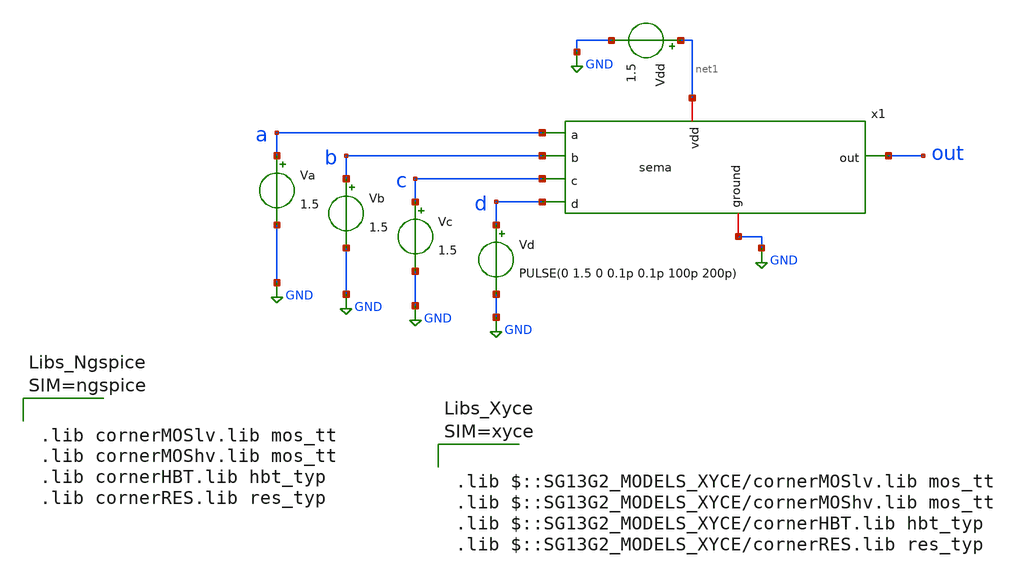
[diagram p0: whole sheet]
** sch_path: projekat/slucaj_3/tb_tran.sch
**.subckt tb_tran
Va a GND 1.5
Vb b GND 1.5
Vc c GND 1.5
Vd d GND PULSE(0 1.5 0 0.1p 0.1p 100p 200p)
Vdd net1 GND 1.5
x1 net1 out d a c b GND sema
**** begin user architecture code



.lib cornerMOSlv.lib mos_tt
.lib cornerMOShv.lib mos_tt
.lib cornerHBT.lib hbt_typ
.lib cornerRES.lib res_typ









.tran 0.1p 500p

.control
  save all
  run

  meas tran tr_out TRIG v(out) VAL=0.15 RISE=2 TARG v(out) VAL=1.35 RISE=2
  meas tran tf_out TRIG v(out) VAL=1.35 FALL=2 TARG v(out) VAL=0.15 FALL=2

  plot v(a)+6 v(b)+4.5 v(c)+3 v(d)+1.5 v(out)
  print tr_out tf_out
.endc

**** end user architecture code
**.ends
.GLOBAL GND
.end
